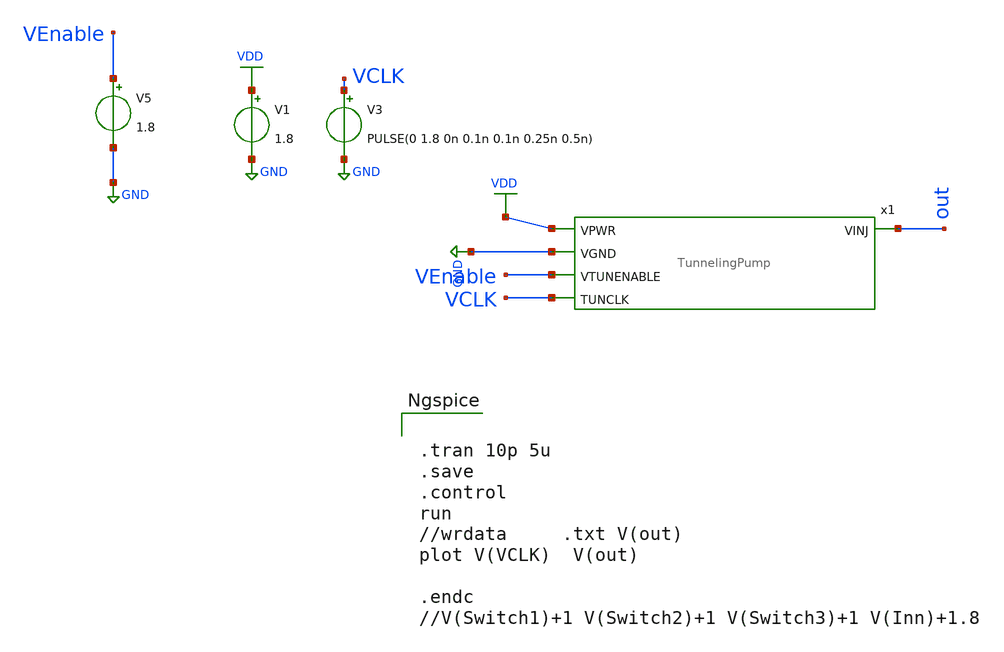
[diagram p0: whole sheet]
** sch_path: sky130_cells/ChargePump/TunnelingPump_TB.sch
**.subckt TunnelingPump_TB
V3 VCLK GND PULSE(0 1.8 0n 0.1n 0.1n 0.25n 0.5n)
V1 VDD GND 1.8
V5 VEnable GND 1.8
x1 out VDD GND VEnable VCLK TunnelingPump
**** begin user architecture code

** opencircuitdesign pdks install
.lib $::SKYWATER_MODELS/sky130.lib.spice tt




.tran 10p 5u
.save
.control
run
//wrdata     .txt V(out)
plot V(VCLK)  V(out)

.endc
//V(Switch1)+1 V(Switch2)+1 V(Switch3)+1 V(Inn)+1.8


**** end user architecture code
**.ends

* expanding   symbol:  sky130_cells/ChargePump/TunnelingPump.sym # of pins=5
** sym_path: sky130_cells/ChargePump/TunnelingPump.sym
** sch_path: sky130_cells/ChargePump/TunnelingPump.sch
.subckt TunnelingPump VINJ VPWR VGND VTUNENABLE TUNCLK
*.ipin VGND
*.ipin VTUNENABLE
*.ipin TUNCLK
*.ipin VPWR
*.opin VINJ
* noconn #net13
* noconn #net14
XM7 net12 VTUNENABLE VPWR VPWR sky130_fd_pr__pfet_01v8 L=0.15 W=1 nf=1 ad='int((nf+1)/2) * W/nf * 0.29'
+ as='int((nf+2)/2) * W/nf * 0.29' pd='2*int((nf+1)/2) * (W/nf + 0.29)' ps='2*int((nf+2)/2) * (W/nf + 0.29)'
+ nrd='0.29 / W' nrs='0.29 / W' sa=0 sb=0 sd=0 mult=1 m=1
XM3 VGND VTUNENABLE net1 VPWR sky130_fd_pr__pfet_01v8 L=0.15 W=1 nf=1 ad='int((nf+1)/2) * W/nf * 0.29'
+ as='int((nf+2)/2) * W/nf * 0.29' pd='2*int((nf+1)/2) * (W/nf + 0.29)' ps='2*int((nf+2)/2) * (W/nf + 0.29)'
+ nrd='0.29 / W' nrs='0.29 / W' sa=0 sb=0 sd=0 mult=1 m=1
XM4 VPWR net12 net1 VPWR sky130_fd_pr__pfet_01v8 L=0.15 W=1 nf=1 ad='int((nf+1)/2) * W/nf * 0.29' as='int((nf+2)/2) * W/nf * 0.29'
+ pd='2*int((nf+1)/2) * (W/nf + 0.29)' ps='2*int((nf+2)/2) * (W/nf + 0.29)' nrd='0.29 / W' nrs='0.29 / W'
+ sa=0 sb=0 sd=0 mult=1 m=1
XM5 net12 VTUNENABLE VGND VGND sky130_fd_pr__nfet_01v8 L=0.15 W=1 nf=1 ad='int((1 + 1)/2) * 1 / 1 * 0.29'
+ as='int((1 + 2)/2) * 1 / 1 * 0.29' pd='2*int((1 + 1)/2) * (1 / 1 + 0.29)' ps='2*int((1 + 2)/2) * (1 / 1 + 0.29)'
+ nrd='0.29 / 1 ' nrs='0.29 / 1 ' sa=0 sb=0 sd=0 mult=1 m=1
XM2 VPWR VTUNENABLE net1 VGND sky130_fd_pr__nfet_01v8 L=0.15 W=1 nf=1 ad='int((1 + 1)/2) * 1 / 1 * 0.29'
+ as='int((1 + 2)/2) * 1 / 1 * 0.29' pd='2*int((1 + 1)/2) * (1 / 1 + 0.29)' ps='2*int((1 + 2)/2) * (1 / 1 + 0.29)'
+ nrd='0.29 / 1 ' nrs='0.29 / 1 ' sa=0 sb=0 sd=0 mult=1 m=1
XM1 VGND net12 net1 VGND sky130_fd_pr__nfet_01v8 L=0.15 W=1 nf=1 ad='int((1 + 1)/2) * 1 / 1 * 0.29' as='int((1 + 2)/2) * 1 / 1 * 0.29'
+ pd='2*int((1 + 1)/2) * (1 / 1 + 0.29)' ps='2*int((1 + 2)/2) * (1 / 1 + 0.29)' nrd='0.29 / 1 ' nrs='0.29 / 1 '
+ sa=0 sb=0 sd=0 mult=1 m=1
D1 net1 net2 sky130_fd_pr__diode_pw2nd_11v0 area=6.831
D3 net2 net4 sky130_fd_pr__diode_pw2nd_11v0 area=6.831
D4 net4 net6 sky130_fd_pr__diode_pw2nd_11v0 area=6.831
D5 net6 net7 sky130_fd_pr__diode_pw2nd_11v0 area=6.831
XC3 net2 net3 sky130_fd_pr__cap_mim_m3_1 W=50 L=5 MF=1 m=1
XC4 net3 net2 sky130_fd_pr__cap_mim_m3_2 W=50 L=5 MF=1 m=1
XC5 net5 net4 sky130_fd_pr__cap_mim_m3_2 W=50 L=5 MF=1 m=1
XC6 net3 net6 sky130_fd_pr__cap_mim_m3_2 W=50 L=5 MF=1 m=1
XC7 net5 net9 sky130_fd_pr__cap_mim_m3_2 W=50 L=5 MF=1 m=1
XC8 VGND VINJ sky130_fd_pr__cap_mim_m3_2 W=96 L=26 MF=1 m=1
XC9 net5 net11 sky130_fd_pr__cap_mim_m3_2 W=50 L=5 MF=1 m=1
XC10 net3 net10 sky130_fd_pr__cap_mim_m3_2 W=50 L=5 MF=1 m=1
XC11 net4 net5 sky130_fd_pr__cap_mim_m3_1 W=50 L=5 MF=1 m=1
XC12 net6 net3 sky130_fd_pr__cap_mim_m3_1 W=50 L=5 MF=1 m=1
XC13 net7 net5 sky130_fd_pr__cap_mim_m3_1 W=50 L=5 MF=1 m=1
XC14 net8 net3 sky130_fd_pr__cap_mim_m3_1 W=50 L=5 MF=1 m=1
XC15 net9 net5 sky130_fd_pr__cap_mim_m3_1 W=50 L=5 MF=1 m=1
XC16 net10 net3 sky130_fd_pr__cap_mim_m3_1 W=50 L=5 MF=1 m=1
XC17 net11 net5 sky130_fd_pr__cap_mim_m3_1 W=50 L=5 MF=1 m=1
XC18 VINJ VGND sky130_fd_pr__cap_mim_m3_1 W=96 L=26 MF=1 m=1
XC19 net3 net8 sky130_fd_pr__cap_mim_m3_2 W=50 L=5 MF=1 m=1
XC20 net5 net7 sky130_fd_pr__cap_mim_m3_2 W=50 L=5 MF=1 m=1
D6 net7 net8 sky130_fd_pr__diode_pw2nd_11v0 area=6.831
D7 net8 net9 sky130_fd_pr__diode_pw2nd_11v0 area=6.831
D8 net9 net10 sky130_fd_pr__diode_pw2nd_11v0 area=6.831
D9 net10 net11 sky130_fd_pr__diode_pw2nd_11v0 area=6.831
D10 net11 VINJ sky130_fd_pr__diode_pw2nd_11v0 area=6.831
x2 VPWR VTUNENABLE TUNCLK net13 net5 VGND net14 net3 clkgen
.ends


* expanding   symbol:  sky130_cells/ChargePump/clkgen.sym # of pins=8
** sym_path: sky130_cells/ChargePump/clkgen.sym
** sch_path: sky130_cells/ChargePump/clkgen.sch
.subckt clkgen VPB ENABLE CLK CLK1B CLK1 VSUBS CLK2B CLK2
*.ipin CLK
*.ipin VPB
*.ipin VSUBS
*.opin CLK1B
*.opin CLK1
*.opin CLK2B
*.opin CLK2
*.ipin ENABLE
XM41 net12 CLK VPB VPB sky130_fd_pr__pfet_01v8_hvt L=0.15 W=1 nf=1 ad='int((1 + 1)/2) * 1 / 1 * 0.29'
+ as='int((1 + 2)/2) * 1 / 1 * 0.29' pd='2*int((1 + 1)/2) * (1 / 1 + 0.29)' ps='2*int((1 + 2)/2) * (1 / 1 + 0.29)'
+ nrd='0.29 / 1 ' nrs='0.29 / 1 ' sa=0 sb=0 sd=0 mult=1 m=1
XM42 net12 ENABLE VPB VPB sky130_fd_pr__pfet_01v8_hvt L=0.15 W=1 nf=1 ad='int((1 + 1)/2) * 1 / 1 * 0.29'
+ as='int((1 + 2)/2) * 1 / 1 * 0.29' pd='2*int((1 + 1)/2) * (1 / 1 + 0.29)' ps='2*int((1 + 2)/2) * (1 / 1 + 0.29)'
+ nrd='0.29 / 1 ' nrs='0.29 / 1 ' sa=0 sb=0 sd=0 mult=1 m=1
XM44 net10 net12 VPB VPB sky130_fd_pr__pfet_01v8_hvt L=0.15 W=1 nf=1 ad='int((1 + 1)/2) * 1 / 1 * 0.29'
+ as='int((1 + 2)/2) * 1 / 1 * 0.29' pd='2*int((1 + 1)/2) * (1 / 1 + 0.29)' ps='2*int((1 + 2)/2) * (1 / 1 + 0.29)'
+ nrd='0.29 / 1 ' nrs='0.29 / 1 ' sa=0 sb=0 sd=0 mult=1 m=1
XM31 net6 A1 VPB VPB sky130_fd_pr__pfet_01v8_hvt L=0.15 W=1 nf=1 ad='int((1 + 1)/2) * 1 / 1 * 0.29' as='int((1 + 2)/2) * 1 / 1 * 0.29'
+ pd='2*int((1 + 1)/2) * (1 / 1 + 0.29)' ps='2*int((1 + 2)/2) * (1 / 1 + 0.29)' nrd='0.29 / 1 ' nrs='0.29 / 1 '
+ sa=0 sb=0 sd=0 mult=1 m=1
XM32 net6 net10 VPB VPB sky130_fd_pr__pfet_01v8_hvt L=0.15 W=1 nf=1 ad='int((1 + 1)/2) * 1 / 1 * 0.29'
+ as='int((1 + 2)/2) * 1 / 1 * 0.29' pd='2*int((1 + 1)/2) * (1 / 1 + 0.29)' ps='2*int((1 + 2)/2) * (1 / 1 + 0.29)'
+ nrd='0.29 / 1 ' nrs='0.29 / 1 ' sa=0 sb=0 sd=0 mult=1 m=1
XM22 p1 net6 VPB VPB sky130_fd_pr__pfet_01v8_hvt L=0.15 W=1 nf=1 ad='int((1 + 1)/2) * 1 / 1 * 0.29' as='int((1 + 2)/2) * 1 / 1 * 0.29'
+ pd='2*int((1 + 1)/2) * (1 / 1 + 0.29)' ps='2*int((1 + 2)/2) * (1 / 1 + 0.29)' nrd='0.29 / 1 ' nrs='0.29 / 1 '
+ sa=0 sb=0 sd=0 mult=3 m=3
XM24 net7 p1 VPB VPB sky130_fd_pr__pfet_01v8_hvt L=0.15 W=1 nf=1 ad='int((1 + 1)/2) * 1 / 1 * 0.29' as='int((1 + 2)/2) * 1 / 1 * 0.29'
+ pd='2*int((1 + 1)/2) * (1 / 1 + 0.29)' ps='2*int((1 + 2)/2) * (1 / 1 + 0.29)' nrd='0.29 / 1 ' nrs='0.29 / 1 '
+ sa=0 sb=0 sd=0 mult=3 m=3
XM26 net8 net7 VPB VPB sky130_fd_pr__pfet_01v8_hvt L=0.15 W=1 nf=1 ad='int((1 + 1)/2) * 1 / 1 * 0.29'
+ as='int((1 + 2)/2) * 1 / 1 * 0.29' pd='2*int((1 + 1)/2) * (1 / 1 + 0.29)' ps='2*int((1 + 2)/2) * (1 / 1 + 0.29)'
+ nrd='0.29 / 1 ' nrs='0.29 / 1 ' sa=0 sb=0 sd=0 mult=3 m=3
XM28 A2 net8 VPB VPB sky130_fd_pr__pfet_01v8_hvt L=0.15 W=1 nf=1 ad='int((1 + 1)/2) * 1 / 1 * 0.29' as='int((1 + 2)/2) * 1 / 1 * 0.29'
+ pd='2*int((1 + 1)/2) * (1 / 1 + 0.29)' ps='2*int((1 + 2)/2) * (1 / 1 + 0.29)' nrd='0.29 / 1 ' nrs='0.29 / 1 '
+ sa=0 sb=0 sd=0 mult=3 m=3
XM2 net1 p1 VPB VPB sky130_fd_pr__pfet_01v8_hvt L=0.15 W=1 nf=1 ad='int((1 + 1)/2) * 1 / 1 * 0.29' as='int((1 + 2)/2) * 1 / 1 * 0.29'
+ pd='2*int((1 + 1)/2) * (1 / 1 + 0.29)' ps='2*int((1 + 2)/2) * (1 / 1 + 0.29)' nrd='0.29 / 1 ' nrs='0.29 / 1 '
+ sa=0 sb=0 sd=0 mult=3 m=3
XM4 CLK1 net1 VPB VPB sky130_fd_pr__pfet_01v8_hvt L=0.15 W=1 nf=1 ad='int((1 + 1)/2) * 1 / 1 * 0.29'
+ as='int((1 + 2)/2) * 1 / 1 * 0.29' pd='2*int((1 + 1)/2) * (1 / 1 + 0.29)' ps='2*int((1 + 2)/2) * (1 / 1 + 0.29)'
+ nrd='0.29 / 1 ' nrs='0.29 / 1 ' sa=0 sb=0 sd=0 mult=3 m=3
XM6 CLK1B CLK1 VPB VPB sky130_fd_pr__pfet_01v8_hvt L=0.15 W=1 nf=1 ad='int((1 + 1)/2) * 1 / 1 * 0.29'
+ as='int((1 + 2)/2) * 1 / 1 * 0.29' pd='2*int((1 + 1)/2) * (1 / 1 + 0.29)' ps='2*int((1 + 2)/2) * (1 / 1 + 0.29)'
+ nrd='0.29 / 1 ' nrs='0.29 / 1 ' sa=0 sb=0 sd=0 mult=3 m=3
XM38 B2 net10 VPB VPB sky130_fd_pr__pfet_01v8_hvt L=0.15 W=1 nf=1 ad='int((1 + 1)/2) * 1 / 1 * 0.29'
+ as='int((1 + 2)/2) * 1 / 1 * 0.29' pd='2*int((1 + 1)/2) * (1 / 1 + 0.29)' ps='2*int((1 + 2)/2) * (1 / 1 + 0.29)'
+ nrd='0.29 / 1 ' nrs='0.29 / 1 ' sa=0 sb=0 sd=0 mult=1 m=1
XM35 net3 A2 VPB VPB sky130_fd_pr__pfet_01v8_hvt L=0.15 W=1 nf=1 ad='int((1 + 1)/2) * 1 / 1 * 0.29' as='int((1 + 2)/2) * 1 / 1 * 0.29'
+ pd='2*int((1 + 1)/2) * (1 / 1 + 0.29)' ps='2*int((1 + 2)/2) * (1 / 1 + 0.29)' nrd='0.29 / 1 ' nrs='0.29 / 1 '
+ sa=0 sb=0 sd=0 mult=1 m=1
XM36 net3 B2 VPB VPB sky130_fd_pr__pfet_01v8_hvt L=0.15 W=1 nf=1 ad='int((1 + 1)/2) * 1 / 1 * 0.29' as='int((1 + 2)/2) * 1 / 1 * 0.29'
+ pd='2*int((1 + 1)/2) * (1 / 1 + 0.29)' ps='2*int((1 + 2)/2) * (1 / 1 + 0.29)' nrd='0.29 / 1 ' nrs='0.29 / 1 '
+ sa=0 sb=0 sd=0 mult=1 m=1
XM14 p2 net3 VPB VPB sky130_fd_pr__pfet_01v8_hvt L=0.15 W=1 nf=1 ad='int((1 + 1)/2) * 1 / 1 * 0.29' as='int((1 + 2)/2) * 1 / 1 * 0.29'
+ pd='2*int((1 + 1)/2) * (1 / 1 + 0.29)' ps='2*int((1 + 2)/2) * (1 / 1 + 0.29)' nrd='0.29 / 1 ' nrs='0.29 / 1 '
+ sa=0 sb=0 sd=0 mult=3 m=3
XM16 net4 p2 VPB VPB sky130_fd_pr__pfet_01v8_hvt L=0.15 W=1 nf=1 ad='int((1 + 1)/2) * 1 / 1 * 0.29' as='int((1 + 2)/2) * 1 / 1 * 0.29'
+ pd='2*int((1 + 1)/2) * (1 / 1 + 0.29)' ps='2*int((1 + 2)/2) * (1 / 1 + 0.29)' nrd='0.29 / 1 ' nrs='0.29 / 1 '
+ sa=0 sb=0 sd=0 mult=3 m=3
XM18 net5 net4 VPB VPB sky130_fd_pr__pfet_01v8_hvt L=0.15 W=1 nf=1 ad='int((1 + 1)/2) * 1 / 1 * 0.29'
+ as='int((1 + 2)/2) * 1 / 1 * 0.29' pd='2*int((1 + 1)/2) * (1 / 1 + 0.29)' ps='2*int((1 + 2)/2) * (1 / 1 + 0.29)'
+ nrd='0.29 / 1 ' nrs='0.29 / 1 ' sa=0 sb=0 sd=0 mult=3 m=3
XM20 A1 net5 VPB VPB sky130_fd_pr__pfet_01v8_hvt L=0.15 W=1 nf=1 ad='int((1 + 1)/2) * 1 / 1 * 0.29' as='int((1 + 2)/2) * 1 / 1 * 0.29'
+ pd='2*int((1 + 1)/2) * (1 / 1 + 0.29)' ps='2*int((1 + 2)/2) * (1 / 1 + 0.29)' nrd='0.29 / 1 ' nrs='0.29 / 1 '
+ sa=0 sb=0 sd=0 mult=3 m=3
XM8 net2 p2 VPB VPB sky130_fd_pr__pfet_01v8_hvt L=0.15 W=1 nf=1 ad='int((1 + 1)/2) * 1 / 1 * 0.29' as='int((1 + 2)/2) * 1 / 1 * 0.29'
+ pd='2*int((1 + 1)/2) * (1 / 1 + 0.29)' ps='2*int((1 + 2)/2) * (1 / 1 + 0.29)' nrd='0.29 / 1 ' nrs='0.29 / 1 '
+ sa=0 sb=0 sd=0 mult=3 m=3
XM10 CLK2 net2 VPB VPB sky130_fd_pr__pfet_01v8_hvt L=0.15 W=1 nf=1 ad='int((1 + 1)/2) * 1 / 1 * 0.29'
+ as='int((1 + 2)/2) * 1 / 1 * 0.29' pd='2*int((1 + 1)/2) * (1 / 1 + 0.29)' ps='2*int((1 + 2)/2) * (1 / 1 + 0.29)'
+ nrd='0.29 / 1 ' nrs='0.29 / 1 ' sa=0 sb=0 sd=0 mult=3 m=3
XM12 CLK2B CLK2 VPB VPB sky130_fd_pr__pfet_01v8_hvt L=0.15 W=1 nf=1 ad='int((1 + 1)/2) * 1 / 1 * 0.29'
+ as='int((1 + 2)/2) * 1 / 1 * 0.29' pd='2*int((1 + 1)/2) * (1 / 1 + 0.29)' ps='2*int((1 + 2)/2) * (1 / 1 + 0.29)'
+ nrd='0.29 / 1 ' nrs='0.29 / 1 ' sa=0 sb=0 sd=0 mult=3 m=3
XM39 net12 ENABLE net13 VSUBS sky130_fd_pr__nfet_01v8 L=0.15 W=0.65 nf=1 ad='int((1 + 1)/2) * 0.65 / 1 * 0.29'
+ as='int((1 + 2)/2) * 0.65 / 1 * 0.29' pd='2*int((1 + 1)/2) * (0.65 / 1 + 0.29)' ps='2*int((1 + 2)/2) * (0.65 / 1 + 0.29)'
+ nrd='0.29 / 0.65 ' nrs='0.29 / 0.65 ' sa=0 sb=0 sd=0 mult=1 m=1
XM40 net13 CLK VSUBS VSUBS sky130_fd_pr__nfet_01v8 L=0.15 W=0.65 nf=1 ad='int((1 + 1)/2) * 0.65 / 1 * 0.29'
+ as='int((1 + 2)/2) * 0.65 / 1 * 0.29' pd='2*int((1 + 1)/2) * (0.65 / 1 + 0.29)' ps='2*int((1 + 2)/2) * (0.65 / 1 + 0.29)'
+ nrd='0.29 / 0.65 ' nrs='0.29 / 0.65 ' sa=0 sb=0 sd=0 mult=1 m=1
XM43 net10 net12 VSUBS VSUBS sky130_fd_pr__nfet_01v8 L=0.15 W=0.65 nf=1 ad='int((1 + 1)/2) * 0.65 / 1 * 0.29'
+ as='int((1 + 2)/2) * 0.65 / 1 * 0.29' pd='2*int((1 + 1)/2) * (0.65 / 1 + 0.29)' ps='2*int((1 + 2)/2) * (0.65 / 1 + 0.29)'
+ nrd='0.29 / 0.65 ' nrs='0.29 / 0.65 ' sa=0 sb=0 sd=0 mult=1 m=1
XM29 net6 A1 net9 VSUBS sky130_fd_pr__nfet_01v8 L=0.15 W=0.65 nf=1 ad='int((1 + 1)/2) * 0.65 / 1 * 0.29'
+ as='int((1 + 2)/2) * 0.65 / 1 * 0.29' pd='2*int((1 + 1)/2) * (0.65 / 1 + 0.29)' ps='2*int((1 + 2)/2) * (0.65 / 1 + 0.29)'
+ nrd='0.29 / 0.65 ' nrs='0.29 / 0.65 ' sa=0 sb=0 sd=0 mult=1 m=1
XM30 net9 net10 VSUBS VSUBS sky130_fd_pr__nfet_01v8 L=0.15 W=0.65 nf=1 ad='int((1 + 1)/2) * 0.65 / 1 * 0.29'
+ as='int((1 + 2)/2) * 0.65 / 1 * 0.29' pd='2*int((1 + 1)/2) * (0.65 / 1 + 0.29)' ps='2*int((1 + 2)/2) * (0.65 / 1 + 0.29)'
+ nrd='0.29 / 0.65 ' nrs='0.29 / 0.65 ' sa=0 sb=0 sd=0 mult=1 m=1
XM21 p1 net6 VSUBS VSUBS sky130_fd_pr__nfet_01v8 L=0.15 W=0.42 nf=1 ad='int((1 + 1)/2) * 0.42 / 1 * 0.29'
+ as='int((1 + 2)/2) * 0.42 / 1 * 0.29' pd='2*int((1 + 1)/2) * (0.42 / 1 + 0.29)' ps='2*int((1 + 2)/2) * (0.42 / 1 + 0.29)'
+ nrd='0.29 / 0.42 ' nrs='0.29 / 0.42 ' sa=0 sb=0 sd=0 mult=2 m=2
XM23 net7 p1 VSUBS VSUBS sky130_fd_pr__nfet_01v8 L=0.15 W=0.42 nf=1 ad='int((1 + 1)/2) * 0.42 / 1 * 0.29'
+ as='int((1 + 2)/2) * 0.42 / 1 * 0.29' pd='2*int((1 + 1)/2) * (0.42 / 1 + 0.29)' ps='2*int((1 + 2)/2) * (0.42 / 1 + 0.29)'
+ nrd='0.29 / 0.42 ' nrs='0.29 / 0.42 ' sa=0 sb=0 sd=0 mult=2 m=2
XM25 net8 net7 VSUBS VSUBS sky130_fd_pr__nfet_01v8 L=0.15 W=0.42 nf=1 ad='int((1 + 1)/2) * 0.42 / 1 * 0.29'
+ as='int((1 + 2)/2) * 0.42 / 1 * 0.29' pd='2*int((1 + 1)/2) * (0.42 / 1 + 0.29)' ps='2*int((1 + 2)/2) * (0.42 / 1 + 0.29)'
+ nrd='0.29 / 0.42 ' nrs='0.29 / 0.42 ' sa=0 sb=0 sd=0 mult=2 m=2
XM27 A2 net8 VSUBS VSUBS sky130_fd_pr__nfet_01v8 L=0.15 W=0.42 nf=1 ad='int((1 + 1)/2) * 0.42 / 1 * 0.29'
+ as='int((1 + 2)/2) * 0.42 / 1 * 0.29' pd='2*int((1 + 1)/2) * (0.42 / 1 + 0.29)' ps='2*int((1 + 2)/2) * (0.42 / 1 + 0.29)'
+ nrd='0.29 / 0.42 ' nrs='0.29 / 0.42 ' sa=0 sb=0 sd=0 mult=2 m=2
XM1 net1 p1 VSUBS VSUBS sky130_fd_pr__nfet_01v8 L=0.15 W=0.42 nf=1 ad='int((1 + 1)/2) * 0.42 / 1 * 0.29'
+ as='int((1 + 2)/2) * 0.42 / 1 * 0.29' pd='2*int((1 + 1)/2) * (0.42 / 1 + 0.29)' ps='2*int((1 + 2)/2) * (0.42 / 1 + 0.29)'
+ nrd='0.29 / 0.42 ' nrs='0.29 / 0.42 ' sa=0 sb=0 sd=0 mult=2 m=2
XM3 CLK1 net1 VSUBS VSUBS sky130_fd_pr__nfet_01v8 L=0.15 W=0.42 nf=1 ad='int((1 + 1)/2) * 0.42 / 1 * 0.29'
+ as='int((1 + 2)/2) * 0.42 / 1 * 0.29' pd='2*int((1 + 1)/2) * (0.42 / 1 + 0.29)' ps='2*int((1 + 2)/2) * (0.42 / 1 + 0.29)'
+ nrd='0.29 / 0.42 ' nrs='0.29 / 0.42 ' sa=0 sb=0 sd=0 mult=2 m=2
XM5 CLK1B CLK1 VSUBS VSUBS sky130_fd_pr__nfet_01v8 L=0.15 W=0.42 nf=1 ad='int((1 + 1)/2) * 0.42 / 1 * 0.29'
+ as='int((1 + 2)/2) * 0.42 / 1 * 0.29' pd='2*int((1 + 1)/2) * (0.42 / 1 + 0.29)' ps='2*int((1 + 2)/2) * (0.42 / 1 + 0.29)'
+ nrd='0.29 / 0.42 ' nrs='0.29 / 0.42 ' sa=0 sb=0 sd=0 mult=2 m=2
XM37 B2 net10 VSUBS VSUBS sky130_fd_pr__nfet_01v8 L=0.15 W=0.65 nf=1 ad='int((1 + 1)/2) * 0.65 / 1 * 0.29'
+ as='int((1 + 2)/2) * 0.65 / 1 * 0.29' pd='2*int((1 + 1)/2) * (0.65 / 1 + 0.29)' ps='2*int((1 + 2)/2) * (0.65 / 1 + 0.29)'
+ nrd='0.29 / 0.65 ' nrs='0.29 / 0.65 ' sa=0 sb=0 sd=0 mult=1 m=1
XM33 net3 A2 net11 VSUBS sky130_fd_pr__nfet_01v8 L=0.15 W=0.65 nf=1 ad='int((1 + 1)/2) * 0.65 / 1 * 0.29'
+ as='int((1 + 2)/2) * 0.65 / 1 * 0.29' pd='2*int((1 + 1)/2) * (0.65 / 1 + 0.29)' ps='2*int((1 + 2)/2) * (0.65 / 1 + 0.29)'
+ nrd='0.29 / 0.65 ' nrs='0.29 / 0.65 ' sa=0 sb=0 sd=0 mult=1 m=1
XM34 net11 B2 VSUBS VSUBS sky130_fd_pr__nfet_01v8 L=0.15 W=0.65 nf=1 ad='int((1 + 1)/2) * 0.65 / 1 * 0.29'
+ as='int((1 + 2)/2) * 0.65 / 1 * 0.29' pd='2*int((1 + 1)/2) * (0.65 / 1 + 0.29)' ps='2*int((1 + 2)/2) * (0.65 / 1 + 0.29)'
+ nrd='0.29 / 0.65 ' nrs='0.29 / 0.65 ' sa=0 sb=0 sd=0 mult=1 m=1
XM13 p2 net3 VSUBS VSUBS sky130_fd_pr__nfet_01v8 L=0.15 W=0.42 nf=1 ad='int((1 + 1)/2) * 0.42 / 1 * 0.29'
+ as='int((1 + 2)/2) * 0.42 / 1 * 0.29' pd='2*int((1 + 1)/2) * (0.42 / 1 + 0.29)' ps='2*int((1 + 2)/2) * (0.42 / 1 + 0.29)'
+ nrd='0.29 / 0.42 ' nrs='0.29 / 0.42 ' sa=0 sb=0 sd=0 mult=2 m=2
XM15 net4 p2 VSUBS VSUBS sky130_fd_pr__nfet_01v8 L=0.15 W=0.42 nf=1 ad='int((1 + 1)/2) * 0.42 / 1 * 0.29'
+ as='int((1 + 2)/2) * 0.42 / 1 * 0.29' pd='2*int((1 + 1)/2) * (0.42 / 1 + 0.29)' ps='2*int((1 + 2)/2) * (0.42 / 1 + 0.29)'
+ nrd='0.29 / 0.42 ' nrs='0.29 / 0.42 ' sa=0 sb=0 sd=0 mult=2 m=2
XM17 net5 net4 VSUBS VSUBS sky130_fd_pr__nfet_01v8 L=0.15 W=0.42 nf=1 ad='int((1 + 1)/2) * 0.42 / 1 * 0.29'
+ as='int((1 + 2)/2) * 0.42 / 1 * 0.29' pd='2*int((1 + 1)/2) * (0.42 / 1 + 0.29)' ps='2*int((1 + 2)/2) * (0.42 / 1 + 0.29)'
+ nrd='0.29 / 0.42 ' nrs='0.29 / 0.42 ' sa=0 sb=0 sd=0 mult=2 m=2
XM19 A1 net5 VSUBS VSUBS sky130_fd_pr__nfet_01v8 L=0.15 W=0.42 nf=1 ad='int((1 + 1)/2) * 0.42 / 1 * 0.29'
+ as='int((1 + 2)/2) * 0.42 / 1 * 0.29' pd='2*int((1 + 1)/2) * (0.42 / 1 + 0.29)' ps='2*int((1 + 2)/2) * (0.42 / 1 + 0.29)'
+ nrd='0.29 / 0.42 ' nrs='0.29 / 0.42 ' sa=0 sb=0 sd=0 mult=2 m=2
XM7 net2 p2 VSUBS VSUBS sky130_fd_pr__nfet_01v8 L=0.15 W=0.42 nf=1 ad='int((1 + 1)/2) * 0.42 / 1 * 0.29'
+ as='int((1 + 2)/2) * 0.42 / 1 * 0.29' pd='2*int((1 + 1)/2) * (0.42 / 1 + 0.29)' ps='2*int((1 + 2)/2) * (0.42 / 1 + 0.29)'
+ nrd='0.29 / 0.42 ' nrs='0.29 / 0.42 ' sa=0 sb=0 sd=0 mult=2 m=2
XM9 CLK2 net2 VSUBS VSUBS sky130_fd_pr__nfet_01v8 L=0.15 W=0.42 nf=1 ad='int((1 + 1)/2) * 0.42 / 1 * 0.29'
+ as='int((1 + 2)/2) * 0.42 / 1 * 0.29' pd='2*int((1 + 1)/2) * (0.42 / 1 + 0.29)' ps='2*int((1 + 2)/2) * (0.42 / 1 + 0.29)'
+ nrd='0.29 / 0.42 ' nrs='0.29 / 0.42 ' sa=0 sb=0 sd=0 mult=2 m=2
XM11 CLK2B CLK2 VSUBS VSUBS sky130_fd_pr__nfet_01v8 L=0.15 W=0.42 nf=1 ad='int((1 + 1)/2) * 0.42 / 1 * 0.29'
+ as='int((1 + 2)/2) * 0.42 / 1 * 0.29' pd='2*int((1 + 1)/2) * (0.42 / 1 + 0.29)' ps='2*int((1 + 2)/2) * (0.42 / 1 + 0.29)'
+ nrd='0.29 / 0.42 ' nrs='0.29 / 0.42 ' sa=0 sb=0 sd=0 mult=2 m=2
.ends

.GLOBAL GND
.GLOBAL VDD
.end
